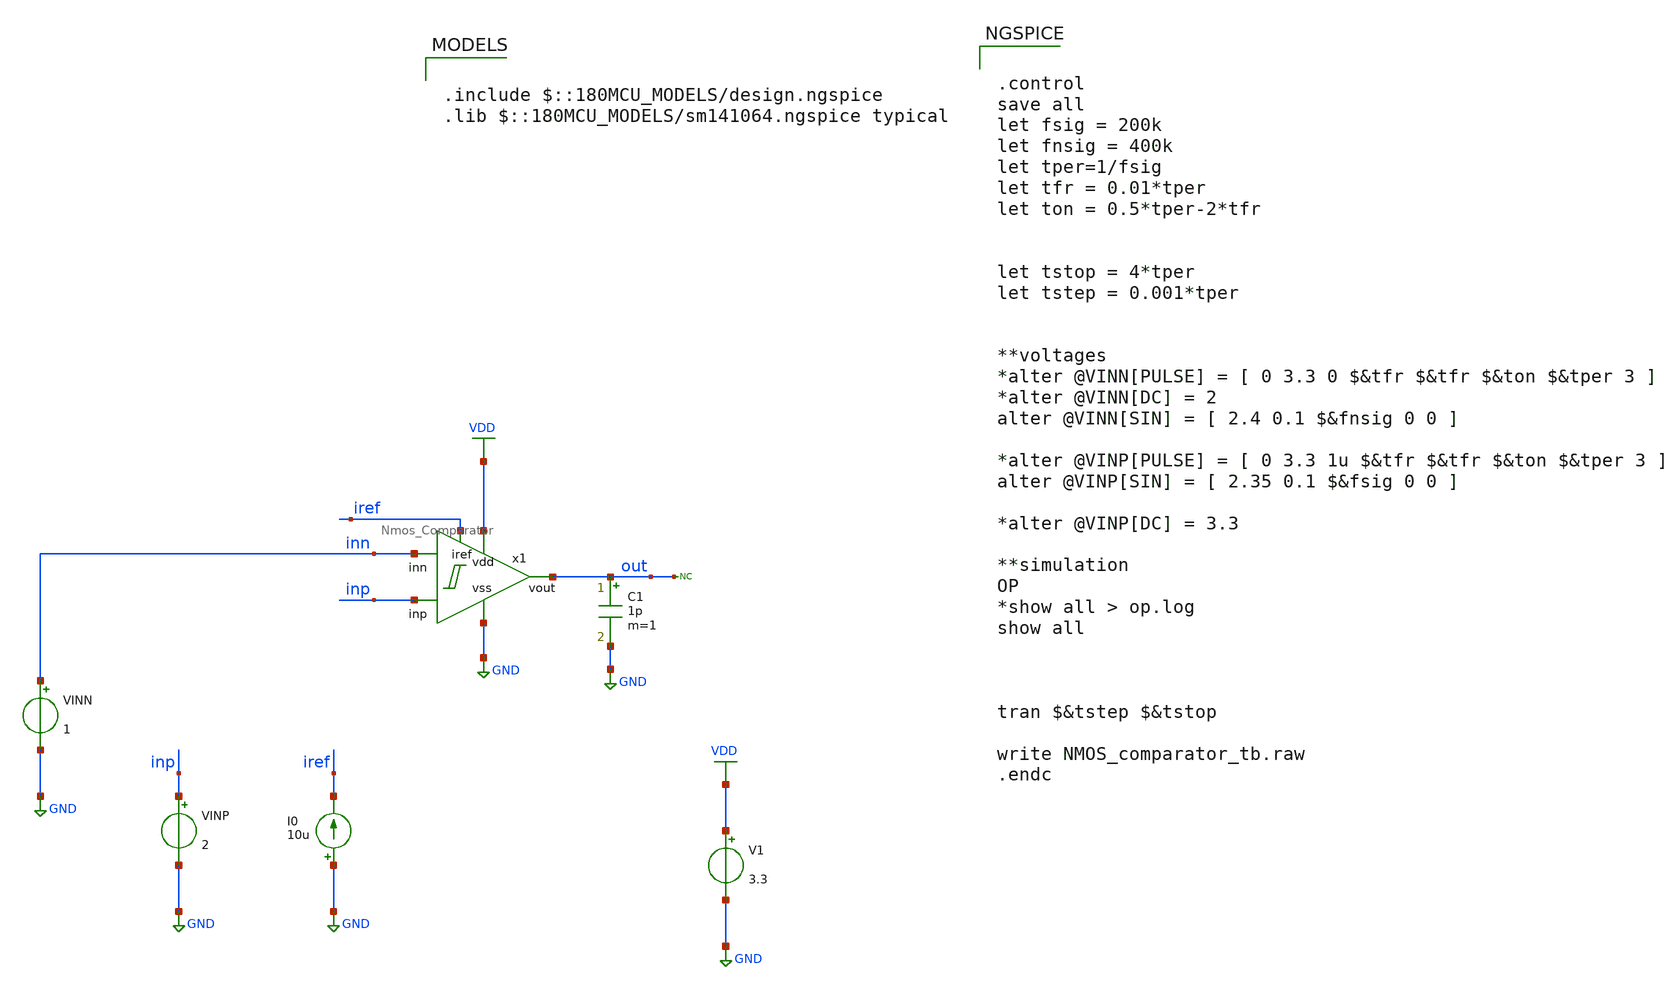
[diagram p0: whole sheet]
** sch_path: designs/switch_matrix_gf180mcu_9t5v0-main/designs/libs/tb_analog/Comparator/NMOS_comparator_tb.sch
**.subckt NMOS_comparator_tb
I0 GND iref 10u
V1 VDD GND 3.3
VINP inp GND 2
* noconn out
VINN inn GND 1
x1 VDD out inp GND inn iref Nmos_Comparator
C1 out GND 1p m=1
**** begin user architecture code


.control
save all
let fsig = 200k
let fnsig = 400k
let tper=1/fsig
let tfr = 0.01*tper
let ton = 0.5*tper-2*tfr


let tstop = 4*tper
let tstep = 0.001*tper


**voltages
*alter @VINN[PULSE] = [ 0 3.3 0 $&tfr $&tfr $&ton $&tper 3 ]
*alter @VINN[DC] = 2
alter @VINN[SIN] = [ 2.4 0.1 $&fnsig 0 0 ]

*alter @VINP[PULSE] = [ 0 3.3 1u $&tfr $&tfr $&ton $&tper 3 ]
alter @VINP[SIN] = [ 2.35 0.1 $&fsig 0 0 ]

*alter @VINP[DC] = 3.3

**simulation
OP
*show all > op.log
show all



tran $&tstep $&tstop

write NMOS_comparator_tb.raw
.endc



.include $::180MCU_MODELS/design.ngspice
.lib $::180MCU_MODELS/sm141064.ngspice typical

**** end user architecture code
**.ends
.GLOBAL GND
.GLOBAL VDD
.end
